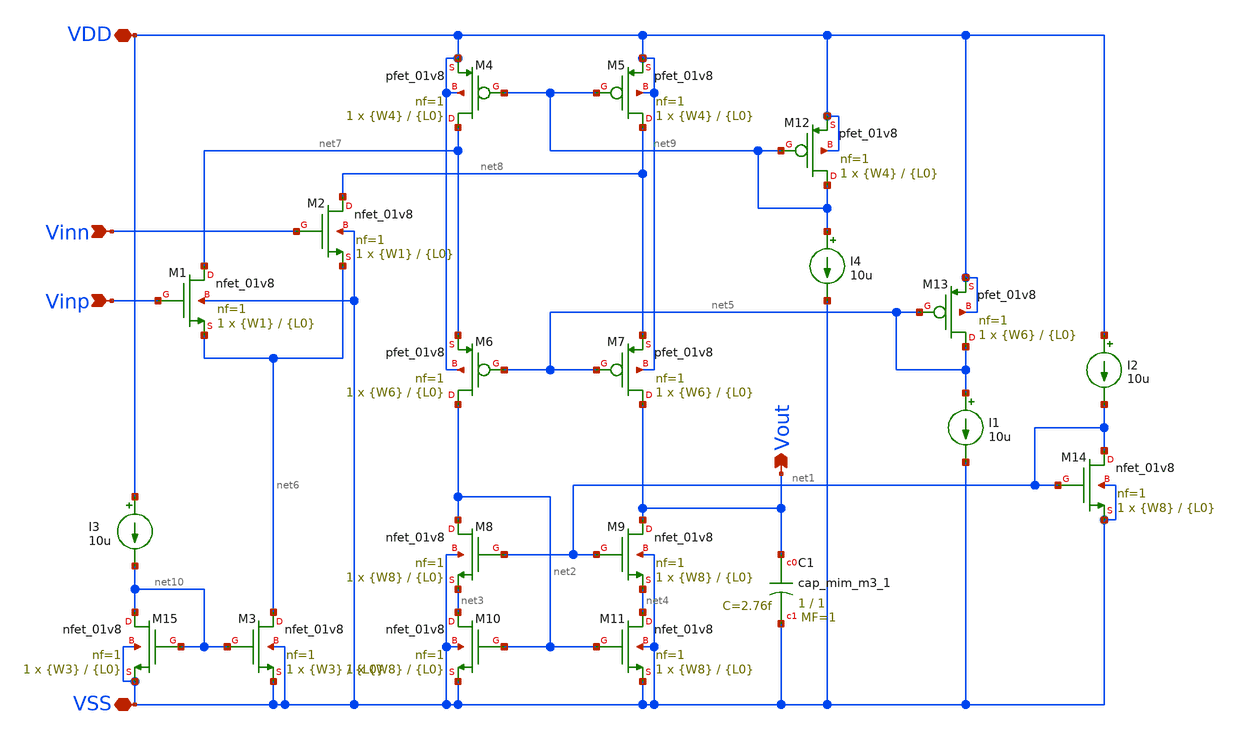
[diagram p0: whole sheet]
** sch_path: opamp_design/folded_cascode_opamp/folded_cascode_opamp.sch
**.subckt folded_cascode_opamp Vout Vinn Vinp VDD VSS
*.opin Vout
*.ipin Vinn
*.ipin Vinp
*.iopin VDD
*.iopin VSS
XM11 net4 net2 VSS VSS sky130_fd_pr__nfet_01v8 L={L0} W={W8} nf=1 ad='int((nf+1)/2) * W/nf * 0.29' as='int((nf+2)/2) * W/nf * 0.29'
+ pd='2*int((nf+1)/2) * (W/nf + 0.29)' ps='2*int((nf+2)/2) * (W/nf + 0.29)' nrd='0.29 / W' nrs='0.29 / W'
+ sa=0 sb=0 sd=0 mult=1 m=1
XM10 net3 net2 VSS VSS sky130_fd_pr__nfet_01v8 L={L0} W={W8} nf=1 ad='int((nf+1)/2) * W/nf * 0.29' as='int((nf+2)/2) * W/nf * 0.29'
+ pd='2*int((nf+1)/2) * (W/nf + 0.29)' ps='2*int((nf+2)/2) * (W/nf + 0.29)' nrd='0.29 / W' nrs='0.29 / W'
+ sa=0 sb=0 sd=0 mult=1 m=1
XM8 net2 net1 net3 VSS sky130_fd_pr__nfet_01v8 L={L0} W={W8} nf=1 ad='int((nf+1)/2) * W/nf * 0.29' as='int((nf+2)/2) * W/nf * 0.29'
+ pd='2*int((nf+1)/2) * (W/nf + 0.29)' ps='2*int((nf+2)/2) * (W/nf + 0.29)' nrd='0.29 / W' nrs='0.29 / W'
+ sa=0 sb=0 sd=0 mult=1 m=1
XM9 Vout net1 net4 VSS sky130_fd_pr__nfet_01v8 L={L0} W={W8} nf=1 ad='int((nf+1)/2) * W/nf * 0.29' as='int((nf+2)/2) * W/nf * 0.29'
+ pd='2*int((nf+1)/2) * (W/nf + 0.29)' ps='2*int((nf+2)/2) * (W/nf + 0.29)' nrd='0.29 / W' nrs='0.29 / W'
+ sa=0 sb=0 sd=0 mult=1 m=1
XM7 Vout net5 net8 VDD sky130_fd_pr__pfet_01v8 L={L0} W={W6} nf=1 ad='int((nf+1)/2) * W/nf * 0.29' as='int((nf+2)/2) * W/nf * 0.29'
+ pd='2*int((nf+1)/2) * (W/nf + 0.29)' ps='2*int((nf+2)/2) * (W/nf + 0.29)' nrd='0.29 / W' nrs='0.29 / W'
+ sa=0 sb=0 sd=0 mult=1 m=1
XM6 net2 net5 net7 VDD sky130_fd_pr__pfet_01v8 L={L0} W={W6} nf=1 ad='int((nf+1)/2) * W/nf * 0.29' as='int((nf+2)/2) * W/nf * 0.29'
+ pd='2*int((nf+1)/2) * (W/nf + 0.29)' ps='2*int((nf+2)/2) * (W/nf + 0.29)' nrd='0.29 / W' nrs='0.29 / W'
+ sa=0 sb=0 sd=0 mult=1 m=1
XM1 net7 Vinp net6 VSS sky130_fd_pr__nfet_01v8 L={L0} W={W1} nf=1 ad='int((nf+1)/2) * W/nf * 0.29' as='int((nf+2)/2) * W/nf * 0.29'
+ pd='2*int((nf+1)/2) * (W/nf + 0.29)' ps='2*int((nf+2)/2) * (W/nf + 0.29)' nrd='0.29 / W' nrs='0.29 / W'
+ sa=0 sb=0 sd=0 mult=1 m=1
XM2 net8 Vinn net6 VSS sky130_fd_pr__nfet_01v8 L={L0} W={W1} nf=1 ad='int((nf+1)/2) * W/nf * 0.29' as='int((nf+2)/2) * W/nf * 0.29'
+ pd='2*int((nf+1)/2) * (W/nf + 0.29)' ps='2*int((nf+2)/2) * (W/nf + 0.29)' nrd='0.29 / W' nrs='0.29 / W'
+ sa=0 sb=0 sd=0 mult=1 m=1
XM3 net6 net10 VSS VSS sky130_fd_pr__nfet_01v8 L={L0} W={W3} nf=1 ad='int((nf+1)/2) * W/nf * 0.29' as='int((nf+2)/2) * W/nf * 0.29'
+ pd='2*int((nf+1)/2) * (W/nf + 0.29)' ps='2*int((nf+2)/2) * (W/nf + 0.29)' nrd='0.29 / W' nrs='0.29 / W'
+ sa=0 sb=0 sd=0 mult=1 m=1
XM4 net7 net9 VDD VDD sky130_fd_pr__pfet_01v8 L={L0} W={W4} nf=1 ad='int((nf+1)/2) * W/nf * 0.29' as='int((nf+2)/2) * W/nf * 0.29'
+ pd='2*int((nf+1)/2) * (W/nf + 0.29)' ps='2*int((nf+2)/2) * (W/nf + 0.29)' nrd='0.29 / W' nrs='0.29 / W'
+ sa=0 sb=0 sd=0 mult=1 m=1
XM5 net8 net9 VDD VDD sky130_fd_pr__pfet_01v8 L={L0} W={W4} nf=1 ad='int((nf+1)/2) * W/nf * 0.29' as='int((nf+2)/2) * W/nf * 0.29'
+ pd='2*int((nf+1)/2) * (W/nf + 0.29)' ps='2*int((nf+2)/2) * (W/nf + 0.29)' nrd='0.29 / W' nrs='0.29 / W'
+ sa=0 sb=0 sd=0 mult=1 m=1
XC1 Vout VSS sky130_fd_pr__cap_mim_m3_1 W=1 L=1 MF=1 m=1
XM12 net9 net9 VDD VDD sky130_fd_pr__pfet_01v8 L={L0} W={W4} nf=1 ad='int((nf+1)/2) * W/nf * 0.29' as='int((nf+2)/2) * W/nf * 0.29'
+ pd='2*int((nf+1)/2) * (W/nf + 0.29)' ps='2*int((nf+2)/2) * (W/nf + 0.29)' nrd='0.29 / W' nrs='0.29 / W'
+ sa=0 sb=0 sd=0 mult=1 m=1
I4 net9 VSS 10u
XM13 net5 net5 VDD VDD sky130_fd_pr__pfet_01v8 L={L0} W={W6} nf=1 ad='int((nf+1)/2) * W/nf * 0.29' as='int((nf+2)/2) * W/nf * 0.29'
+ pd='2*int((nf+1)/2) * (W/nf + 0.29)' ps='2*int((nf+2)/2) * (W/nf + 0.29)' nrd='0.29 / W' nrs='0.29 / W'
+ sa=0 sb=0 sd=0 mult=1 m=1
I1 net5 VSS 10u
XM14 net1 net1 VSS VSS sky130_fd_pr__nfet_01v8 L={L0} W={W8} nf=1 ad='int((nf+1)/2) * W/nf * 0.29' as='int((nf+2)/2) * W/nf * 0.29'
+ pd='2*int((nf+1)/2) * (W/nf + 0.29)' ps='2*int((nf+2)/2) * (W/nf + 0.29)' nrd='0.29 / W' nrs='0.29 / W'
+ sa=0 sb=0 sd=0 mult=1 m=1
I2 VDD net1 10u
XM15 net10 net10 VSS VSS sky130_fd_pr__nfet_01v8 L={L0} W={W3} nf=1 ad='int((nf+1)/2) * W/nf * 0.29'
+ as='int((nf+2)/2) * W/nf * 0.29' pd='2*int((nf+1)/2) * (W/nf + 0.29)' ps='2*int((nf+2)/2) * (W/nf + 0.29)'
+ nrd='0.29 / W' nrs='0.29 / W' sa=0 sb=0 sd=0 mult=1 m=1
I3 VDD net10 10u
**.ends
.end
